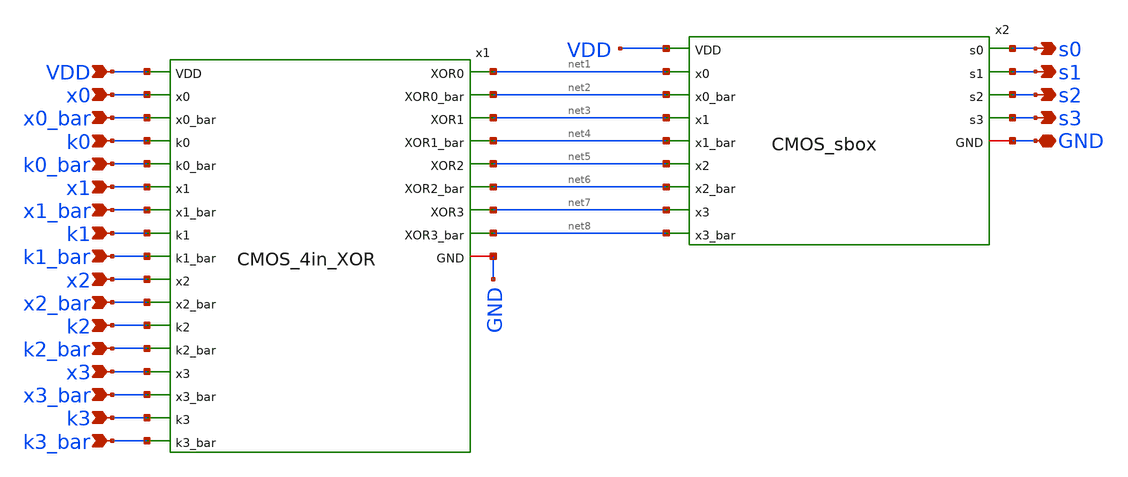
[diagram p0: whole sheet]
** sch_path: skywater_stuff/untitled-17.sch
**.subckt untitled-17 x0 x0_bar k0 k0_bar x1 x1_bar k1 k1_bar x2 x2_bar k2 k2_bar x3 x3_bar k3
*+ k3_bar GND s0 s2 s3 s1 VDD
*.ipin x0
*.ipin x0_bar
*.ipin k0
*.ipin k0_bar
*.ipin x1
*.ipin x1_bar
*.ipin k1
*.ipin k1_bar
*.ipin x2
*.ipin x2_bar
*.ipin k2
*.ipin k2_bar
*.ipin x3
*.ipin x3_bar
*.ipin k3
*.ipin k3_bar
*.iopin GND
*.opin s0
*.opin s2
*.opin s3
*.opin s1
*.ipin VDD
x1 VDD net1 x0 net2 x0_bar k0 k0_bar net3 x1 net4 x1_bar k1 k1_bar net5 x2 x2_bar net6 k2 k2_bar
+ net7 x3 GND net8 x3_bar k3 k3_bar CMOS_4in_XOR
x2 s0 VDD net1 net2 net3 net4 net5 net6 net7 net8 s1 s2 s3 GND CMOS_sbox
**.ends
.end
